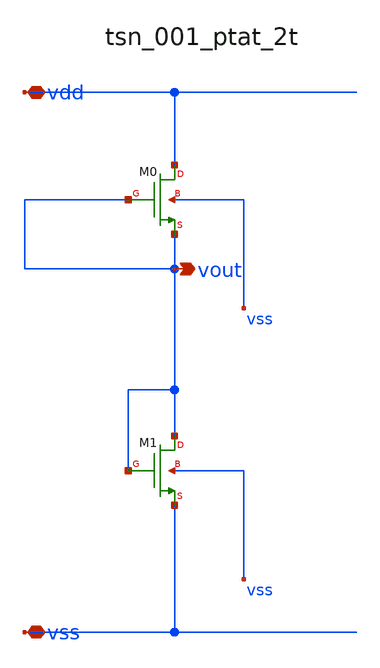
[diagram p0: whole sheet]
** sch_path: analog-db/raw/tsn_001_ptat_2t/tsn_001_ptat_2t.sch
**.subckt tsn_001_ptat_2t vdd vss vout
*.iopin vdd
*.iopin vss
*.opin vout
XM0 vdd vout vout vss sg13_lv_nmos w=x_dut_xm0_w l=x_dut_xm0_l ng=1 m=x_dut_xm0_m
XM1 vout vout vss vss sg13_lv_nmos w=x_dut_xm1_w l=x_dut_xm1_l ng=1 m=x_dut_xm1_m
**.ends
.end
